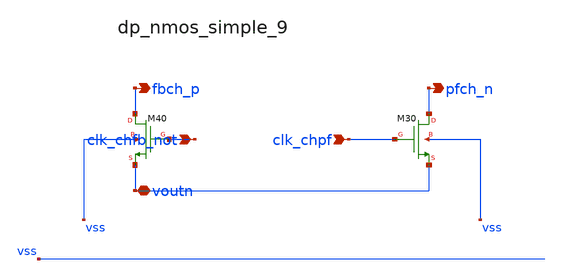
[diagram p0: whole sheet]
** sch_path: analog-db/raw/ia_003_fan_chopper_pf/hier/blocks/dp_nmos_simple_9.sch
**.subckt dp_nmos_simple_9 clk_chfb_not clk_chpf voutn fbch_p pfch_n
*.ipin clk_chfb_not
*.ipin clk_chpf
*.iopin voutn
*.opin fbch_p
*.opin pfch_n
XM30 pfch_n clk_chpf voutn vss sg13_lv_nmos w=x_dut_xm30_w l=x_dut_xm30_l ng=1 m=x_dut_xm30_m
XM40 fbch_p clk_chfb_not voutn vss sg13_lv_nmos w=x_dut_xm40_w l=x_dut_xm40_l ng=1 m=x_dut_xm40_m
**.ends
.end
